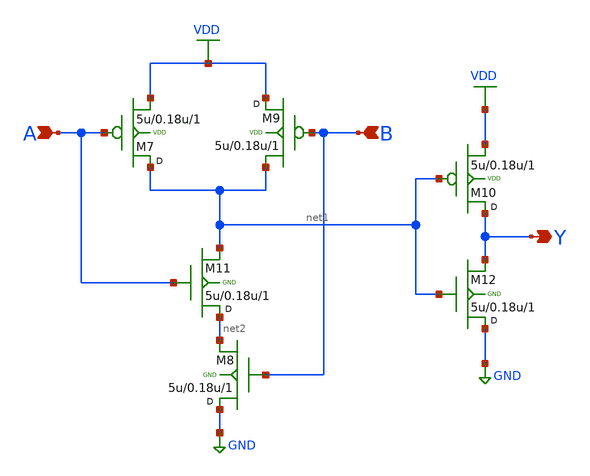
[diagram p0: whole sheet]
** sch_path: sch/AND2_0a.sch
**.subckt AND2_0a A B Y
*.ipin A
*.ipin B
*.opin Y
M7 net1 A VDD VDD pfet w=5u l=0.18u m=1
M8 GND B net2 GND nfet w=5u l=0.18u m=1
M9 VDD B net1 VDD pfet w=5u l=0.18u m=1
M10 Y net1 VDD VDD pfet w=5u l=0.18u m=1
M11 net2 A net1 GND nfet w=5u l=0.18u m=1
M12 GND net1 Y GND nfet w=5u l=0.18u m=1
**.ends
.GLOBAL GND
.GLOBAL VDD
.end
